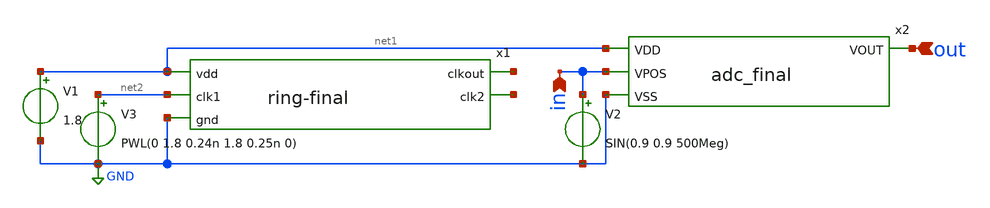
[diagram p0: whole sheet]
** sch_path: week4/xschem/analog_tb.sch
**.subckt analog_tb out in
*.ipin out
*.ipin in
x1 net1 net3 net2 net4 GND ring-final
x2 out net1 in GND adc_final
V1 net1 GND 1.8
V3 net2 GND PWL(0 1.8 0.24n 1.8 0.25n 0)
V2 in GND SIN(0.9 0.9 500Meg)
**** begin user architecture code


.lib /usr/local/share/pdk/sky130A/libs.tech/ngspice/sky130.lib.spice tt
.control
	tran 0.01n 4n
	plot v(in) v(out)
.endc
.save all


**** end user architecture code
**.ends

* expanding   symbol:  ring-final.sym # of pins=5
** sym_path: week4/xschem/ring-final.sym
** sch_path: week4/xschem/ring-final.sch
.subckt ring-final vdd clkout clk1 clk2 gnd
*.ipin vdd
*.ipin gnd
*.ipin clk1
*.opin clkout
*.opin clk2
XM7 vdd clk1 clkin gnd sky130_fd_pr__nfet_01v8 L=0.15 W=1 nf=1 ad='int((nf+1)/2) * W/nf * 0.29' as='int((nf+2)/2) * W/nf * 0.29'
+ pd='2*int((nf+1)/2) * (W/nf + 0.29)' ps='2*int((nf+2)/2) * (W/nf + 0.29)' nrd='0.29 / W' nrs='0.29 / W'
+ sa=0 sb=0 sd=0 mult=1 m=1
XM8 clk2 clk1 gnd gnd sky130_fd_pr__nfet_01v8 L=0.15 W=1 nf=1 ad='int((nf+1)/2) * W/nf * 0.29' as='int((nf+2)/2) * W/nf * 0.29'
+ pd='2*int((nf+1)/2) * (W/nf + 0.29)' ps='2*int((nf+2)/2) * (W/nf + 0.29)' nrd='0.29 / W' nrs='0.29 / W'
+ sa=0 sb=0 sd=0 mult=1 m=1
XM9 clk2 clk1 vdd vdd sky130_fd_pr__pfet_01v8 L=0.15 W=1 nf=1 ad='int((nf+1)/2) * W/nf * 0.29' as='int((nf+2)/2) * W/nf * 0.29'
+ pd='2*int((nf+1)/2) * (W/nf + 0.29)' ps='2*int((nf+2)/2) * (W/nf + 0.29)' nrd='0.29 / W' nrs='0.29 / W'
+ sa=0 sb=0 sd=0 mult=1 m=1
XM10 clkout clk2 clkin gnd sky130_fd_pr__nfet_01v8 L=0.15 W=1 nf=1 ad='int((nf+1)/2) * W/nf * 0.29' as='int((nf+2)/2) * W/nf * 0.29'
+ pd='2*int((nf+1)/2) * (W/nf + 0.29)' ps='2*int((nf+2)/2) * (W/nf + 0.29)' nrd='0.29 / W' nrs='0.29 / W'
+ sa=0 sb=0 sd=0 mult=1 m=1
XM1 net1 clkin gnd gnd sky130_fd_pr__nfet_01v8 L=0.15 W=1 nf=1 ad='int((nf+1)/2) * W/nf * 0.29' as='int((nf+2)/2) * W/nf * 0.29'
+ pd='2*int((nf+1)/2) * (W/nf + 0.29)' ps='2*int((nf+2)/2) * (W/nf + 0.29)' nrd='0.29 / W' nrs='0.29 / W'
+ sa=0 sb=0 sd=0 mult=1 m=1
XM2 net1 clkin vdd vdd sky130_fd_pr__pfet_01v8 L=0.15 W=3 nf=1 ad='int((nf+1)/2) * W/nf * 0.29' as='int((nf+2)/2) * W/nf * 0.29'
+ pd='2*int((nf+1)/2) * (W/nf + 0.29)' ps='2*int((nf+2)/2) * (W/nf + 0.29)' nrd='0.29 / W' nrs='0.29 / W'
+ sa=0 sb=0 sd=0 mult=1 m=1
XM3 net2 net1 gnd gnd sky130_fd_pr__nfet_01v8 L=0.15 W=1 nf=1 ad='int((nf+1)/2) * W/nf * 0.29' as='int((nf+2)/2) * W/nf * 0.29'
+ pd='2*int((nf+1)/2) * (W/nf + 0.29)' ps='2*int((nf+2)/2) * (W/nf + 0.29)' nrd='0.29 / W' nrs='0.29 / W'
+ sa=0 sb=0 sd=0 mult=1 m=1
XM4 net2 net1 vdd vdd sky130_fd_pr__pfet_01v8 L=0.15 W=6 nf=1 ad='int((nf+1)/2) * W/nf * 0.29' as='int((nf+2)/2) * W/nf * 0.29'
+ pd='2*int((nf+1)/2) * (W/nf + 0.29)' ps='2*int((nf+2)/2) * (W/nf + 0.29)' nrd='0.29 / W' nrs='0.29 / W'
+ sa=0 sb=0 sd=0 mult=1 m=1
XM5 clkout net3 gnd gnd sky130_fd_pr__nfet_01v8 L=0.15 W=1 nf=1 ad='int((nf+1)/2) * W/nf * 0.29' as='int((nf+2)/2) * W/nf * 0.29'
+ pd='2*int((nf+1)/2) * (W/nf + 0.29)' ps='2*int((nf+2)/2) * (W/nf + 0.29)' nrd='0.29 / W' nrs='0.29 / W'
+ sa=0 sb=0 sd=0 mult=1 m=1
XM6 clkout net3 vdd vdd sky130_fd_pr__pfet_01v8 L=0.15 W=48 nf=1 ad='int((nf+1)/2) * W/nf * 0.29' as='int((nf+2)/2) * W/nf * 0.29'
+ pd='2*int((nf+1)/2) * (W/nf + 0.29)' ps='2*int((nf+2)/2) * (W/nf + 0.29)' nrd='0.29 / W' nrs='0.29 / W'
+ sa=0 sb=0 sd=0 mult=1 m=1
XM11 net4 net2 gnd gnd sky130_fd_pr__nfet_01v8 L=0.15 W=1 nf=1 ad='int((nf+1)/2) * W/nf * 0.29' as='int((nf+2)/2) * W/nf * 0.29'
+ pd='2*int((nf+1)/2) * (W/nf + 0.29)' ps='2*int((nf+2)/2) * (W/nf + 0.29)' nrd='0.29 / W' nrs='0.29 / W'
+ sa=0 sb=0 sd=0 mult=1 m=1
XM12 net4 net2 vdd vdd sky130_fd_pr__pfet_01v8 L=0.15 W=12 nf=1 ad='int((nf+1)/2) * W/nf * 0.29' as='int((nf+2)/2) * W/nf * 0.29'
+ pd='2*int((nf+1)/2) * (W/nf + 0.29)' ps='2*int((nf+2)/2) * (W/nf + 0.29)' nrd='0.29 / W' nrs='0.29 / W'
+ sa=0 sb=0 sd=0 mult=1 m=1
XM13 net3 net4 gnd gnd sky130_fd_pr__nfet_01v8 L=0.15 W=1 nf=1 ad='int((nf+1)/2) * W/nf * 0.29' as='int((nf+2)/2) * W/nf * 0.29'
+ pd='2*int((nf+1)/2) * (W/nf + 0.29)' ps='2*int((nf+2)/2) * (W/nf + 0.29)' nrd='0.29 / W' nrs='0.29 / W'
+ sa=0 sb=0 sd=0 mult=1 m=1
XM14 net3 net4 vdd vdd sky130_fd_pr__pfet_01v8 L=0.15 W=24 nf=1 ad='int((nf+1)/2) * W/nf * 0.29' as='int((nf+2)/2) * W/nf * 0.29'
+ pd='2*int((nf+1)/2) * (W/nf + 0.29)' ps='2*int((nf+2)/2) * (W/nf + 0.29)' nrd='0.29 / W' nrs='0.29 / W'
+ sa=0 sb=0 sd=0 mult=1 m=1
.ends


* expanding   symbol:  adc_final.sym # of pins=4
** sym_path: week4/xschem/adc_final.sym
** sch_path: week4/xschem/adc_final.sch
.subckt adc_final VOUT VDD VPOS VSS
*.ipin VDD
*.opin VOUT
*.ipin VSS
*.ipin VPOS
XM1 VREF VREF VSS VSS sky130_fd_pr__nfet_01v8 L=0.15 W=1 nf=1 ad='int((nf+1)/2) * W/nf * 0.29' as='int((nf+2)/2) * W/nf * 0.29'
+ pd='2*int((nf+1)/2) * (W/nf + 0.29)' ps='2*int((nf+2)/2) * (W/nf + 0.29)' nrd='0.29 / W' nrs='0.29 / W'
+ sa=0 sb=0 sd=0 mult=1 m=1
XM2 VREF VREF VDD VDD sky130_fd_pr__pfet_01v8 L=0.15 W=1 nf=1 ad='int((nf+1)/2) * W/nf * 0.29' as='int((nf+2)/2) * W/nf * 0.29'
+ pd='2*int((nf+1)/2) * (W/nf + 0.29)' ps='2*int((nf+2)/2) * (W/nf + 0.29)' nrd='0.29 / W' nrs='0.29 / W'
+ sa=0 sb=0 sd=0 mult=1 m=1
XM3 net1 VREF VDD VDD sky130_fd_pr__pfet_01v8 L=0.15 W=3 nf=1 ad='int((nf+1)/2) * W/nf * 0.29' as='int((nf+2)/2) * W/nf * 0.29'
+ pd='2*int((nf+1)/2) * (W/nf + 0.29)' ps='2*int((nf+2)/2) * (W/nf + 0.29)' nrd='0.29 / W' nrs='0.29 / W'
+ sa=0 sb=0 sd=0 mult=1 m=1
XM4 net2 VREF net1 VDD sky130_fd_pr__pfet_01v8 L=0.15 W=3 nf=1 ad='int((nf+1)/2) * W/nf * 0.29' as='int((nf+2)/2) * W/nf * 0.29'
+ pd='2*int((nf+1)/2) * (W/nf + 0.29)' ps='2*int((nf+2)/2) * (W/nf + 0.29)' nrd='0.29 / W' nrs='0.29 / W'
+ sa=0 sb=0 sd=0 mult=1 m=1
XM5 DIFF VPOS net1 VDD sky130_fd_pr__pfet_01v8 L=0.15 W=3 nf=1 ad='int((nf+1)/2) * W/nf * 0.29' as='int((nf+2)/2) * W/nf * 0.29'
+ pd='2*int((nf+1)/2) * (W/nf + 0.29)' ps='2*int((nf+2)/2) * (W/nf + 0.29)' nrd='0.29 / W' nrs='0.29 / W'
+ sa=0 sb=0 sd=0 mult=1 m=1
XM6 net2 net2 VSS VSS sky130_fd_pr__nfet_01v8 L=0.15 W=1 nf=1 ad='int((nf+1)/2) * W/nf * 0.29' as='int((nf+2)/2) * W/nf * 0.29'
+ pd='2*int((nf+1)/2) * (W/nf + 0.29)' ps='2*int((nf+2)/2) * (W/nf + 0.29)' nrd='0.29 / W' nrs='0.29 / W'
+ sa=0 sb=0 sd=0 mult=1 m=1
XM7 DIFF net2 VSS VSS sky130_fd_pr__nfet_01v8 L=0.15 W=1 nf=1 ad='int((nf+1)/2) * W/nf * 0.29' as='int((nf+2)/2) * W/nf * 0.29'
+ pd='2*int((nf+1)/2) * (W/nf + 0.29)' ps='2*int((nf+2)/2) * (W/nf + 0.29)' nrd='0.29 / W' nrs='0.29 / W'
+ sa=0 sb=0 sd=0 mult=1 m=1
XM8 VOUT DIFF VSS VSS sky130_fd_pr__nfet_01v8 L=0.15 W=1 nf=1 ad='int((nf+1)/2) * W/nf * 0.29' as='int((nf+2)/2) * W/nf * 0.29'
+ pd='2*int((nf+1)/2) * (W/nf + 0.29)' ps='2*int((nf+2)/2) * (W/nf + 0.29)' nrd='0.29 / W' nrs='0.29 / W'
+ sa=0 sb=0 sd=0 mult=1 m=1
XM9 VOUT VREF VDD VDD sky130_fd_pr__pfet_01v8 L=0.15 W=6 nf=1 ad='int((nf+1)/2) * W/nf * 0.29' as='int((nf+2)/2) * W/nf * 0.29'
+ pd='2*int((nf+1)/2) * (W/nf + 0.29)' ps='2*int((nf+2)/2) * (W/nf + 0.29)' nrd='0.29 / W' nrs='0.29 / W'
+ sa=0 sb=0 sd=0 mult=1 m=1
XM10 VOUT DIFF VOUT VSS sky130_fd_pr__nfet_01v8 L=0.15 W=1 nf=1 ad='int((nf+1)/2) * W/nf * 0.29' as='int((nf+2)/2) * W/nf * 0.29'
+ pd='2*int((nf+1)/2) * (W/nf + 0.29)' ps='2*int((nf+2)/2) * (W/nf + 0.29)' nrd='0.29 / W' nrs='0.29 / W'
+ sa=0 sb=0 sd=0 mult=1 m=1
.ends

.GLOBAL GND
.end
